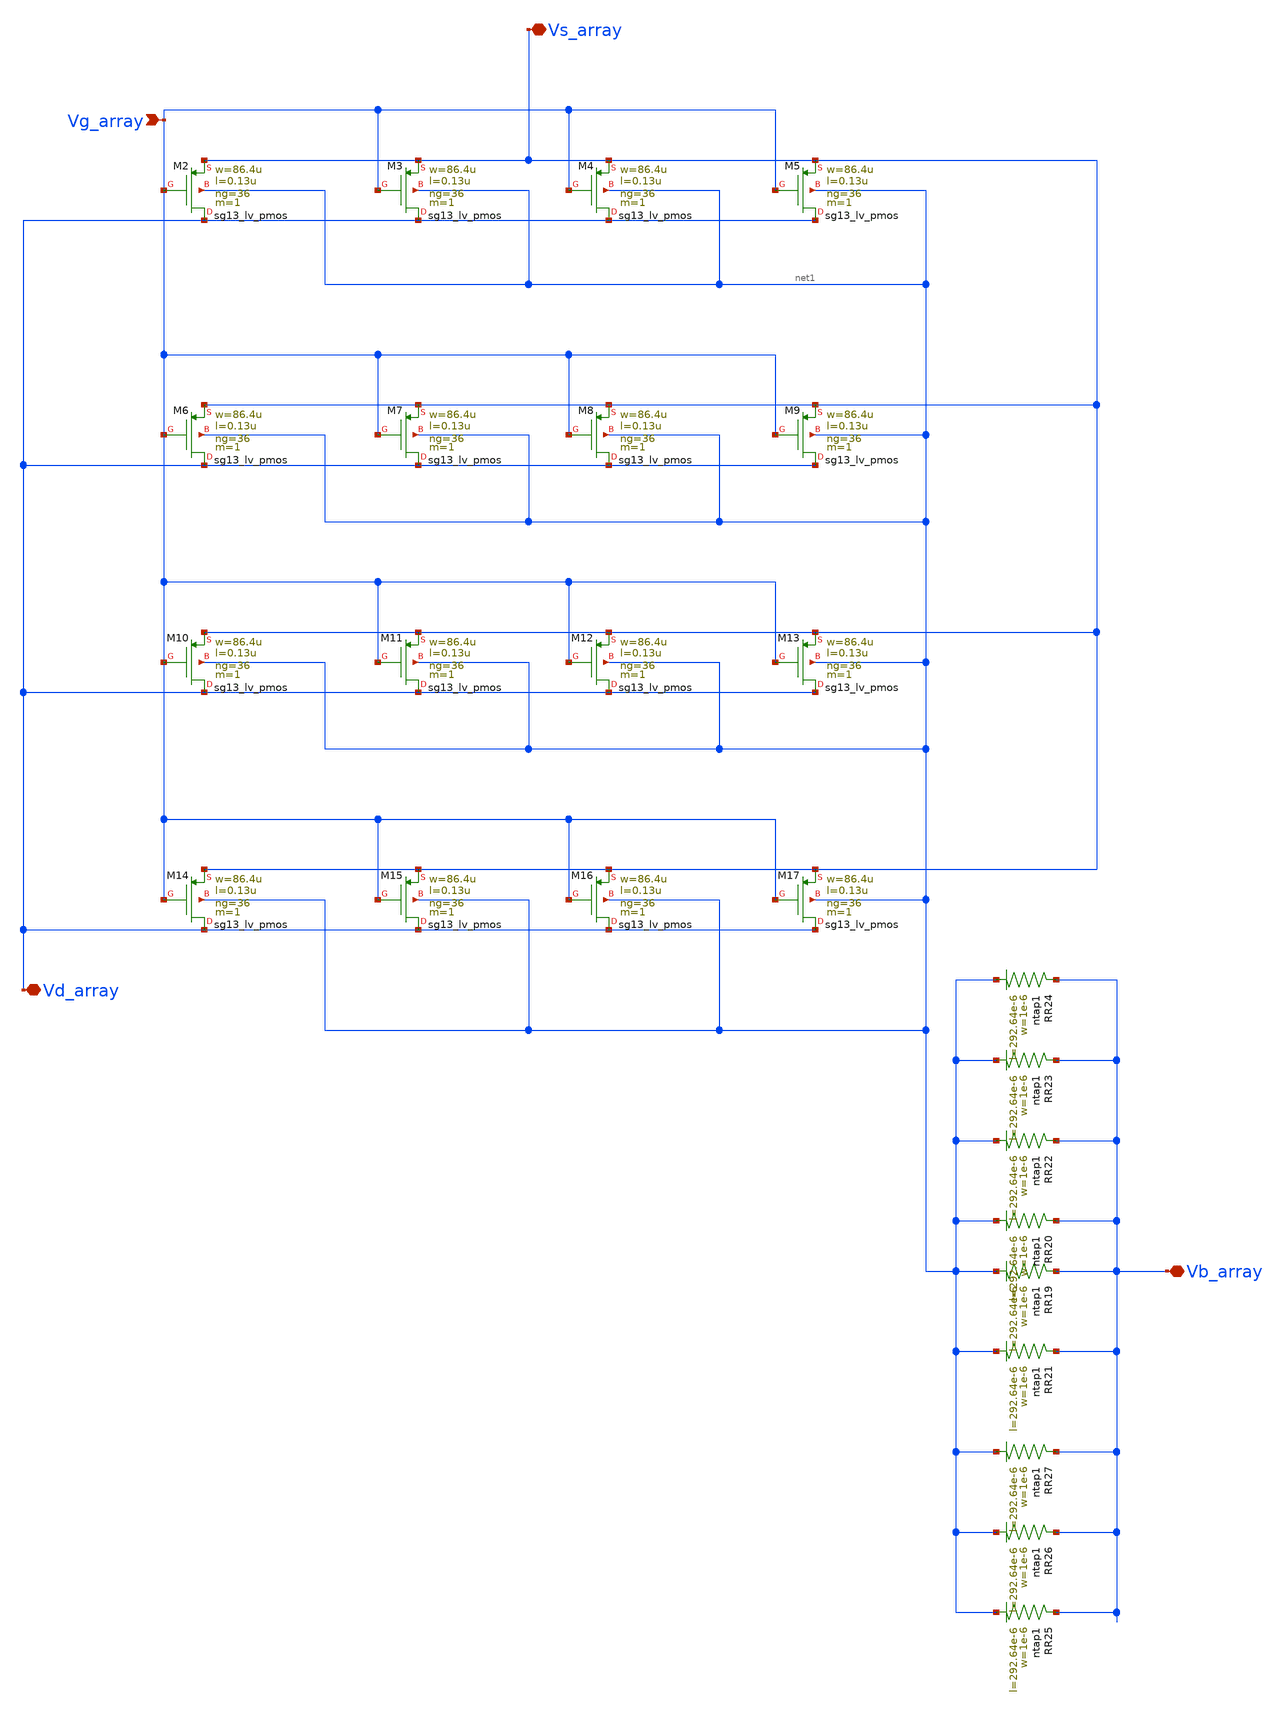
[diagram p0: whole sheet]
** sch_path: Layouts/PMOS/pmos_array_matrix.sch
**.subckt pmos_array_matrix Vg_array Vs_array Vd_array Vb_array
*.ipin Vg_array
*.iopin Vs_array
*.iopin Vd_array
*.iopin Vb_array
XM2 Vd_array Vg_array Vs_array net1 sg13_lv_pmos w=86.4u l=0.13u ng=36 m=1 mm_ok=1
XM3 Vd_array Vg_array Vs_array net1 sg13_lv_pmos w=86.4u l=0.13u ng=36 m=1 mm_ok=1
XM4 Vd_array Vg_array Vs_array net1 sg13_lv_pmos w=86.4u l=0.13u ng=36 m=1 mm_ok=1
XM5 Vd_array Vg_array Vs_array net1 sg13_lv_pmos w=86.4u l=0.13u ng=36 m=1 mm_ok=1
XM6 Vd_array Vg_array Vs_array net1 sg13_lv_pmos w=86.4u l=0.13u ng=36 m=1 mm_ok=1
XM7 Vd_array Vg_array Vs_array net1 sg13_lv_pmos w=86.4u l=0.13u ng=36 m=1 mm_ok=1
XM8 Vd_array Vg_array Vs_array net1 sg13_lv_pmos w=86.4u l=0.13u ng=36 m=1 mm_ok=1
XM9 Vd_array Vg_array Vs_array net1 sg13_lv_pmos w=86.4u l=0.13u ng=36 m=1 mm_ok=1
XM10 Vd_array Vg_array Vs_array net1 sg13_lv_pmos w=86.4u l=0.13u ng=36 m=1 mm_ok=1
XM11 Vd_array Vg_array Vs_array net1 sg13_lv_pmos w=86.4u l=0.13u ng=36 m=1 mm_ok=1
XM12 Vd_array Vg_array Vs_array net1 sg13_lv_pmos w=86.4u l=0.13u ng=36 m=1 mm_ok=1
XM13 Vd_array Vg_array Vs_array net1 sg13_lv_pmos w=86.4u l=0.13u ng=36 m=1 mm_ok=1
XM14 Vd_array Vg_array Vs_array net1 sg13_lv_pmos w=86.4u l=0.13u ng=36 m=1 mm_ok=1
XM15 Vd_array Vg_array Vs_array net1 sg13_lv_pmos w=86.4u l=0.13u ng=36 m=1 mm_ok=1
XM16 Vd_array Vg_array Vs_array net1 sg13_lv_pmos w=86.4u l=0.13u ng=36 m=1 mm_ok=1
XM17 Vd_array Vg_array Vs_array net1 sg13_lv_pmos w=86.4u l=0.13u ng=36 m=1 mm_ok=1
XR19 Vb_array net1 ntap1 R=1.114 w=1e-6 l=292.64e-6
XR20 Vb_array net1 ntap1 R=1.114 w=1e-6 l=292.64e-6
XR21 Vb_array net1 ntap1 R=1.114 w=1e-6 l=292.64e-6
XR22 Vb_array net1 ntap1 R=1.114 w=1e-6 l=292.64e-6
XR23 Vb_array net1 ntap1 R=1.114 w=1e-6 l=292.64e-6
XR24 Vb_array net1 ntap1 R=1.114 w=1e-6 l=292.64e-6
XR25 Vb_array net1 ntap1 R=1.114 w=1e-6 l=292.64e-6
XR26 Vb_array net1 ntap1 R=1.114 w=1e-6 l=292.64e-6
XR27 Vb_array net1 ntap1 R=1.114 w=1e-6 l=292.64e-6
**.ends
.end
